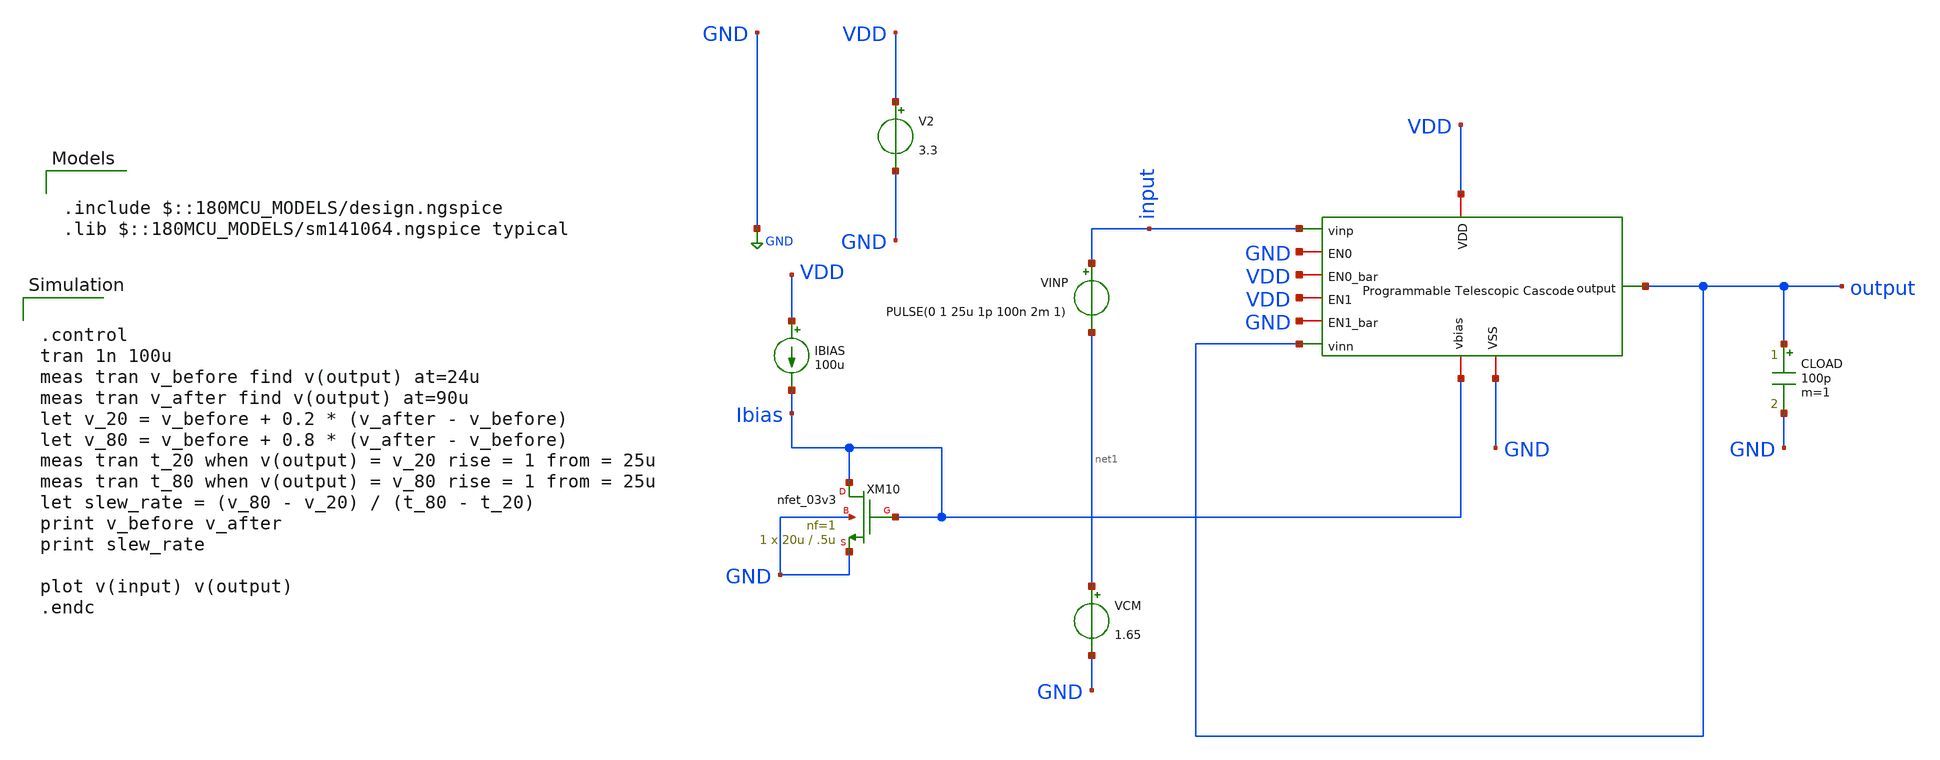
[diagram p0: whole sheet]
** sch_path: designs/libs/core_amps/ota_telescopic/programmable tb/programmable_telescopic_tran_SR_tb.sch
**.subckt programmable_telescopic_tran_SR_tb
V2 VDD GND 3.3
CLOAD output GND 100p m=1
VINP input net1 PULSE(0 1 25u 1p 100n 2m 1)
VCM net1 GND 1.65
x1 VDD output GND VDD VDD GND output input GND Ibias programmable_telescopic_cascode
IBIAS VDD Ibias 100u
XM10 Ibias Ibias GND GND nfet_03v3 L=.5u W=20u nf=1 ad='int((nf+1)/2) * W/nf * 0.18u' as='int((nf+2)/2) * W/nf * 0.18u'
+ pd='2*int((nf+1)/2) * (W/nf + 0.18u)' ps='2*int((nf+2)/2) * (W/nf + 0.18u)' nrd='0.18u / W' nrs='0.18u / W'
+ sa=0 sb=0 sd=0 m=1
**** begin user architecture code

.include $::180MCU_MODELS/design.ngspice
.lib $::180MCU_MODELS/sm141064.ngspice typical



.control
tran 1n 100u
meas tran v_before find v(output) at=24u
meas tran v_after find v(output) at=90u
let v_20 = v_before + 0.2 * (v_after - v_before)
let v_80 = v_before + 0.8 * (v_after - v_before)
meas tran t_20 when v(output) = v_20 rise = 1 from = 25u
meas tran t_80 when v(output) = v_80 rise = 1 from = 25u
let slew_rate = (v_80 - v_20) / (t_80 - t_20)
print v_before v_after
print slew_rate

plot v(input) v(output)
.endc



**** end user architecture code
**.ends
.GLOBAL GND
.end
